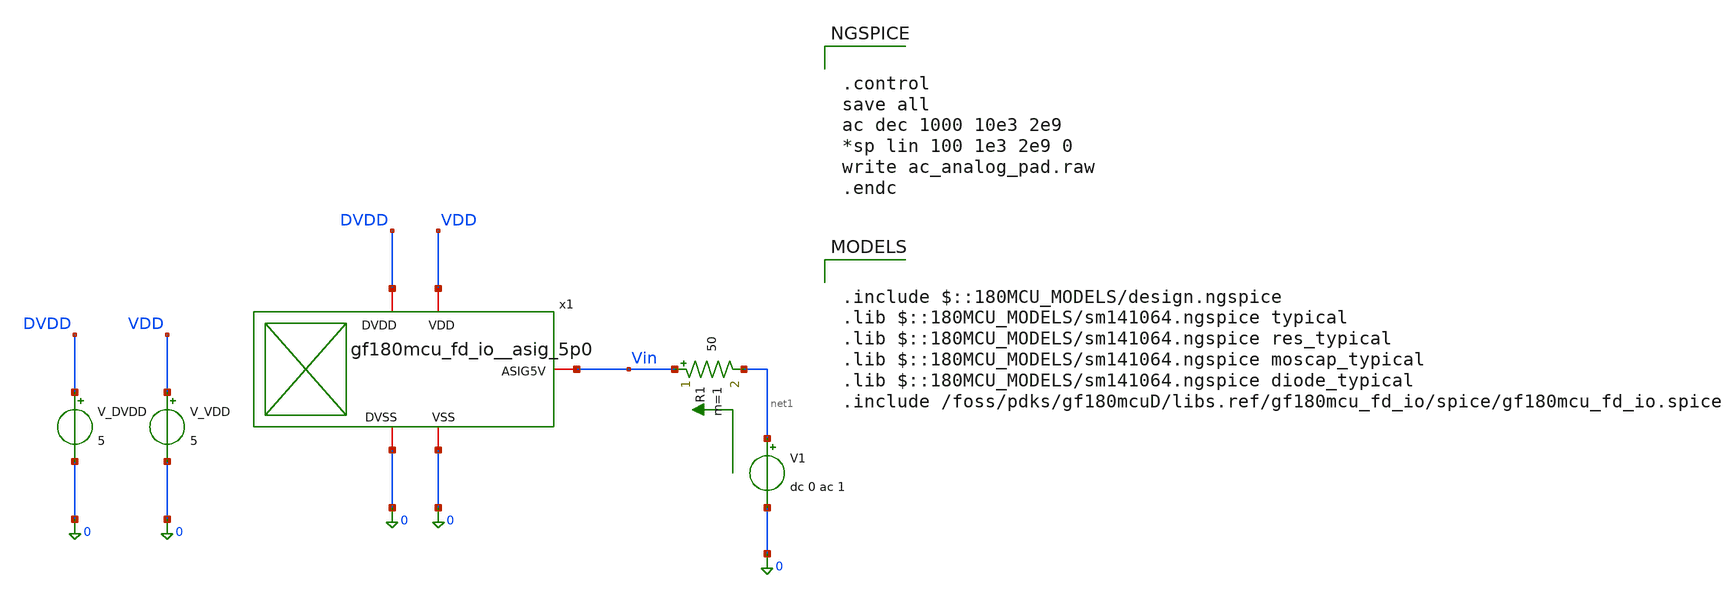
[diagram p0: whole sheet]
** sch_path: Pads_Simulation/schematic_ac.sch
**.subckt schematic_ac
x1 Vin DVDD 0 VDD 0 gf180mcu_fd_io__asig_5p0
V1 net1 0 dc 0 ac 1
V_VDD VDD 0 5
V_DVDD DVDD 0 5
R1 Vin net1 50 m=1
**** begin user architecture code


.control
save all
ac dec 1000 10e3 2e9
*sp lin 100 1e3 2e9 0
write ac_analog_pad.raw
.endc



.include $::180MCU_MODELS/design.ngspice
.lib $::180MCU_MODELS/sm141064.ngspice typical
.lib $::180MCU_MODELS/sm141064.ngspice res_typical
.lib $::180MCU_MODELS/sm141064.ngspice moscap_typical
.lib $::180MCU_MODELS/sm141064.ngspice diode_typical
.include /foss/pdks/gf180mcuD/libs.ref/gf180mcu_fd_io/spice/gf180mcu_fd_io.spice

**** end user architecture code
**.ends
.end
